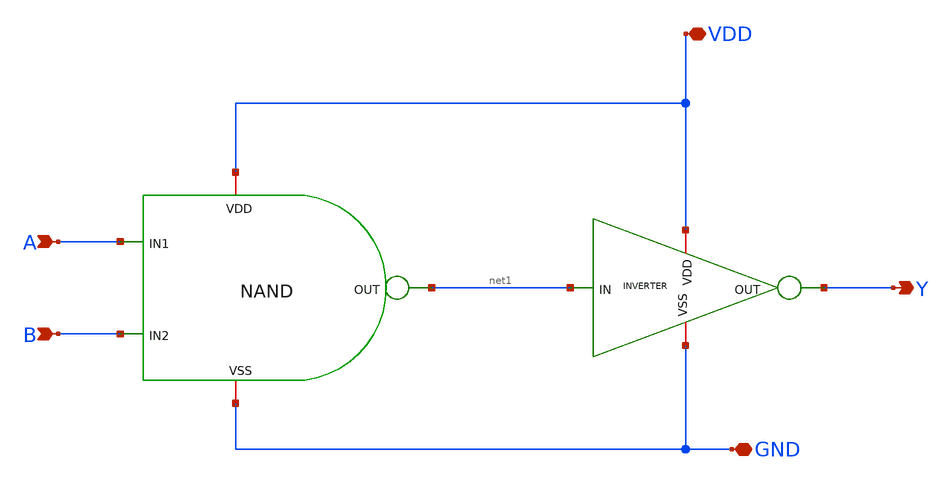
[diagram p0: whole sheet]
** sch_path: DECODER3TO8/Schematic/AND.sch
**.subckt AND A B Y VDD GND
*.ipin A
*.ipin B
*.opin Y
*.iopin VDD
*.iopin GND
x1 VDD net1 A B GND NAND
x2 VDD net1 Y GND INVERTER
**.ends
.end
